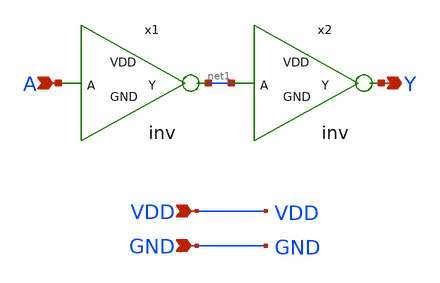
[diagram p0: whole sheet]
** sch_path: xschem/buf.sch
**.subckt buf A Y VDD GND
*.ipin A
*.opin Y
*.ipin VDD
*.ipin GND
x1 A net1 GND VDD inv
x2 net1 Y GND VDD inv
**** begin user architecture code

** opencircuitdesign pdks install
.lib $::SKYWATER_MODELS/sky130.lib.spice tt


**** end user architecture code
**.ends

* expanding   symbol:  inv.sym # of pins=2
** sym_path: xschem/inv.sym
** sch_path: xschem/inv.sch
.subckt inv A Y GND VDD
*.opin Y
*.ipin A
XM1 Y A VDD VDD sky130_fd_pr__pfet_01v8 L=0.15 W=0.42 nf=1 ad='int((nf+1)/2) * W/nf * 0.29' as='int((nf+2)/2) * W/nf * 0.29'
+ pd='2*int((nf+1)/2) * (W/nf + 0.29)' ps='2*int((nf+2)/2) * (W/nf + 0.29)' nrd='0.29 / W' nrs='0.29 / W'
+ sa=0 sb=0 sd=0 mult=1 m=1
XM2 Y A GND GND sky130_fd_pr__nfet_01v8 L=0.15 W=0.42 nf=1 ad='int((nf+1)/2) * W/nf * 0.29' as='int((nf+2)/2) * W/nf * 0.29'
+ pd='2*int((nf+1)/2) * (W/nf + 0.29)' ps='2*int((nf+2)/2) * (W/nf + 0.29)' nrd='0.29 / W' nrs='0.29 / W'
+ sa=0 sb=0 sd=0 mult=1 m=1
.ends

.GLOBAL VDD
.GLOBAL GND
.end
